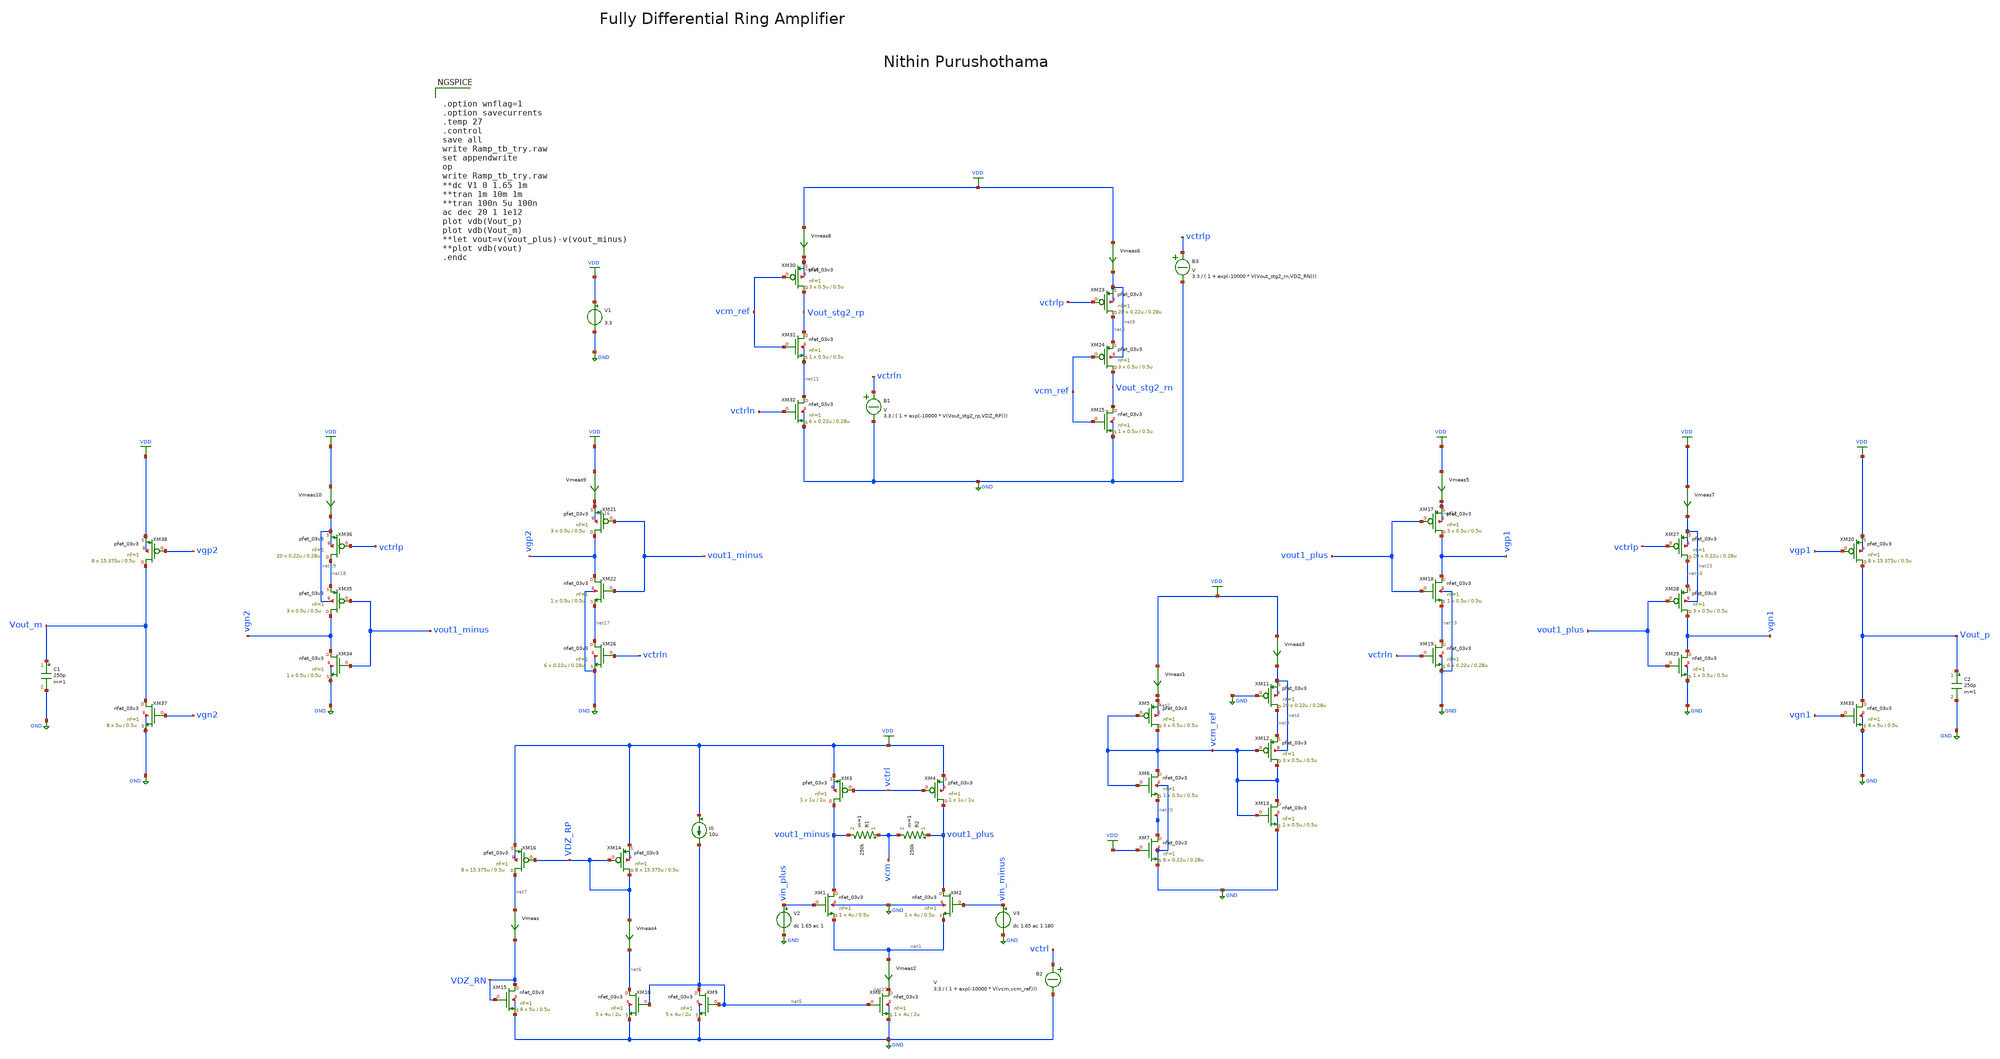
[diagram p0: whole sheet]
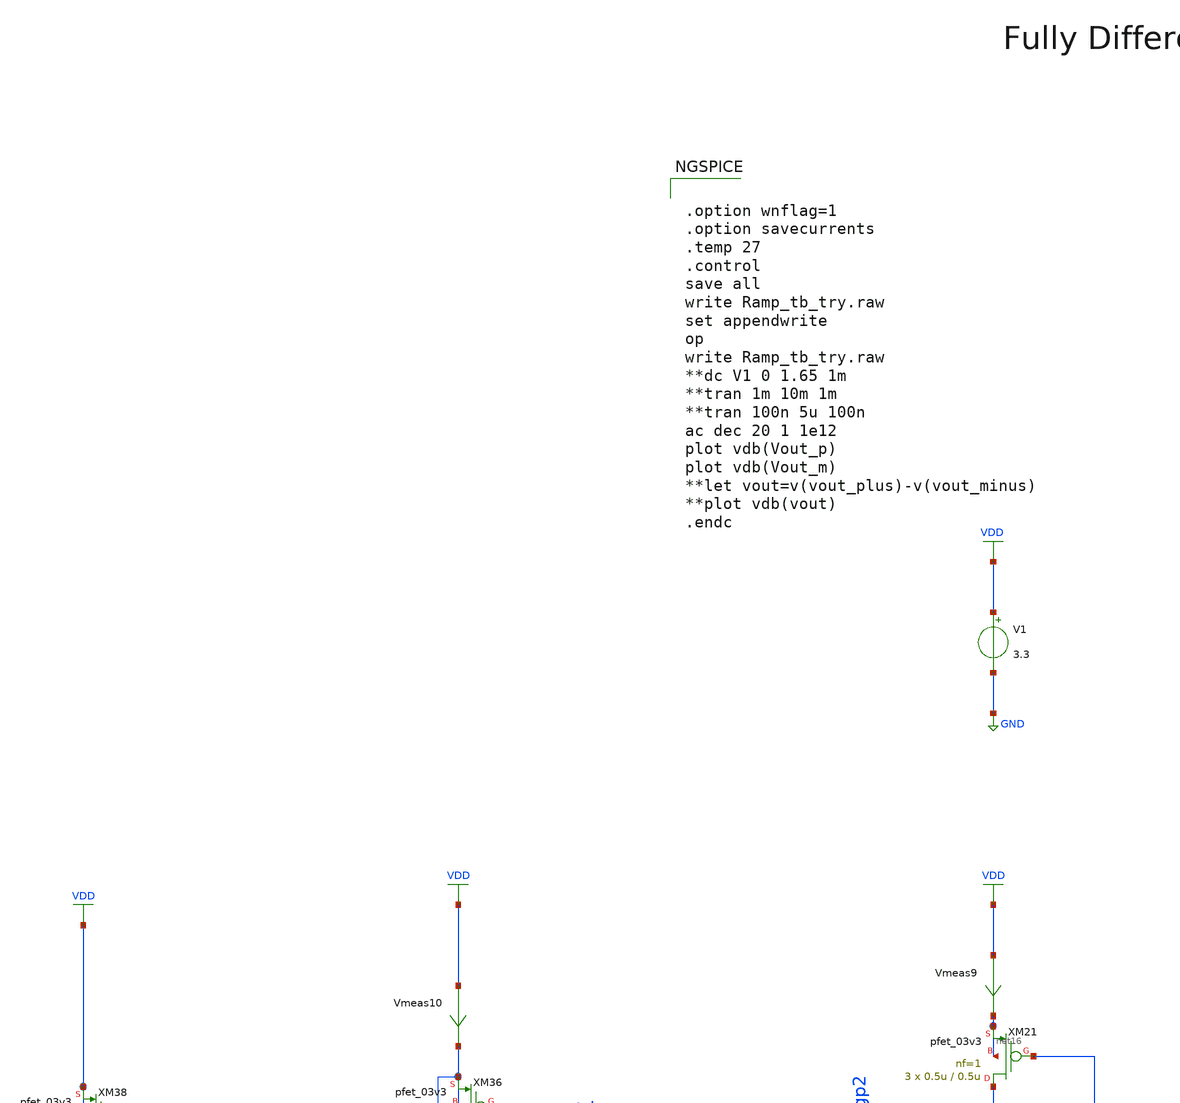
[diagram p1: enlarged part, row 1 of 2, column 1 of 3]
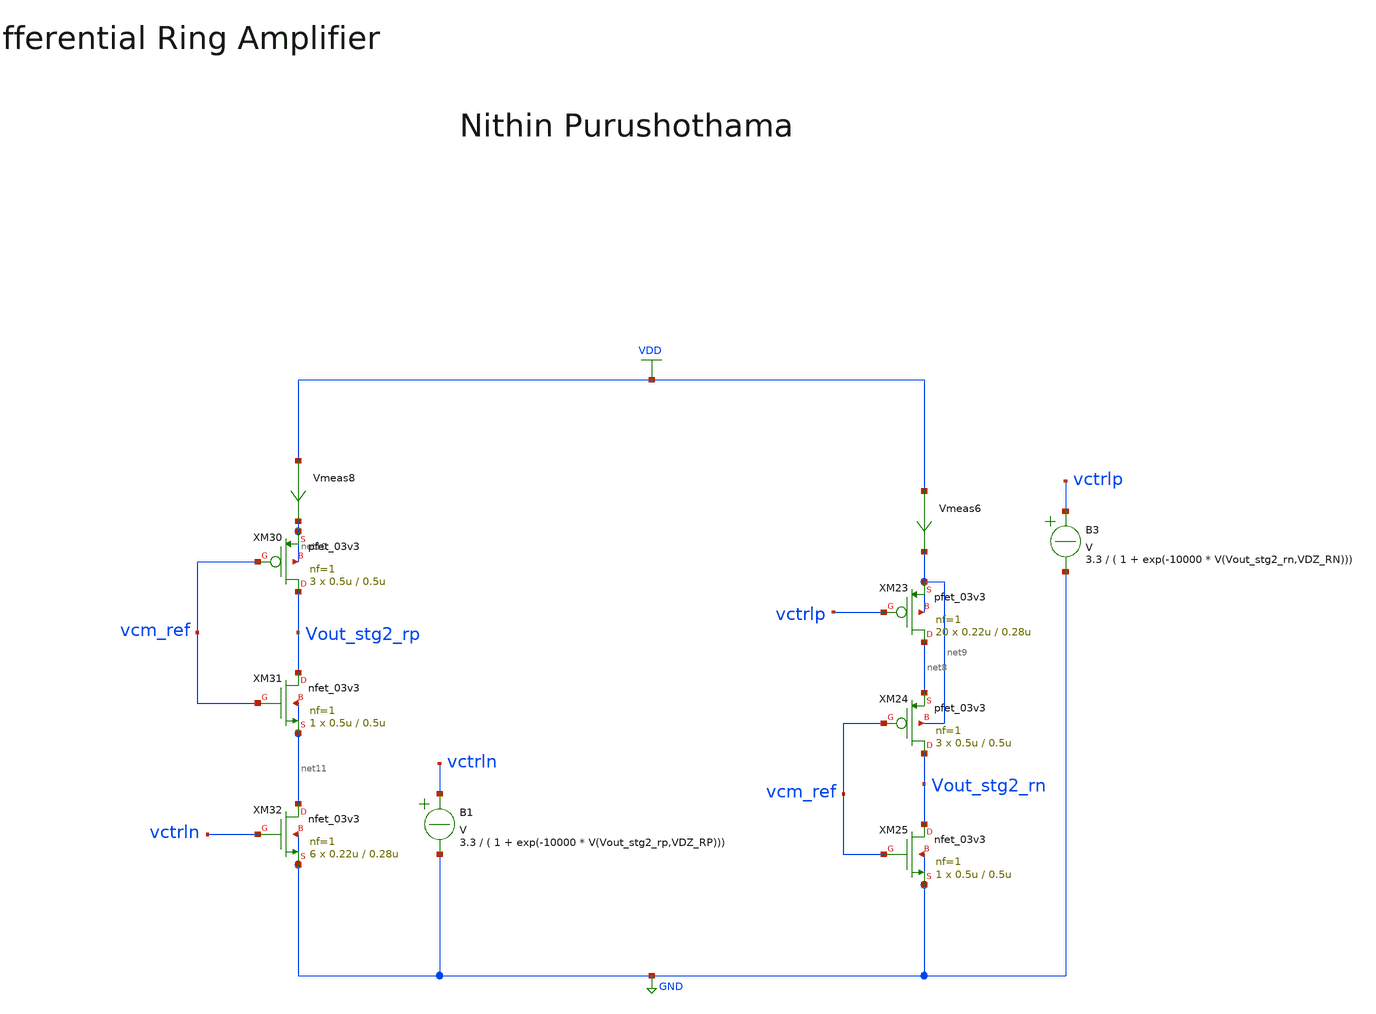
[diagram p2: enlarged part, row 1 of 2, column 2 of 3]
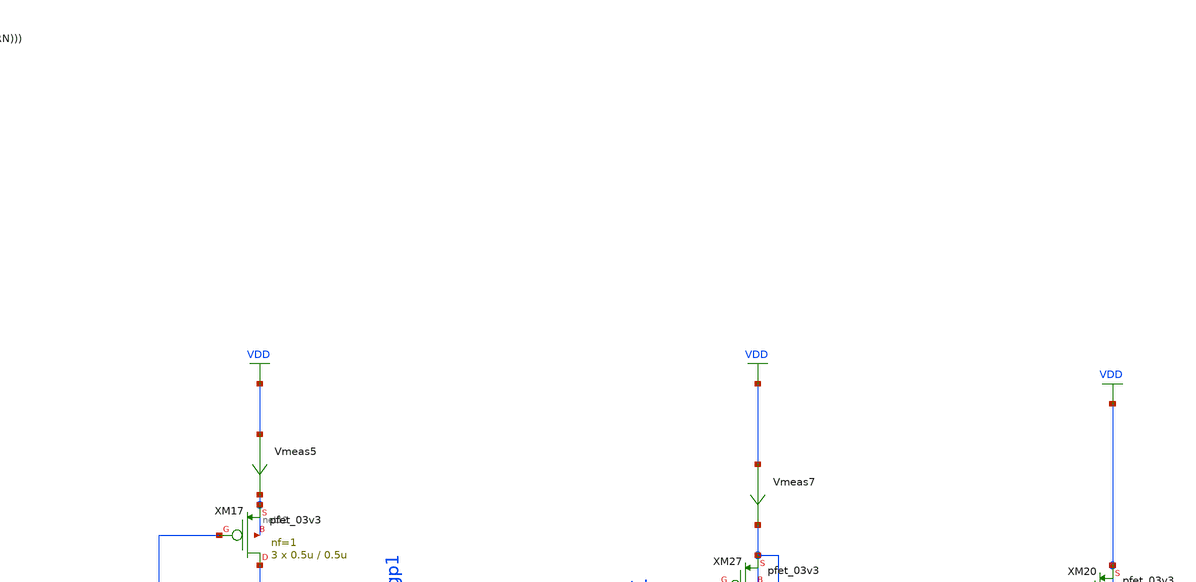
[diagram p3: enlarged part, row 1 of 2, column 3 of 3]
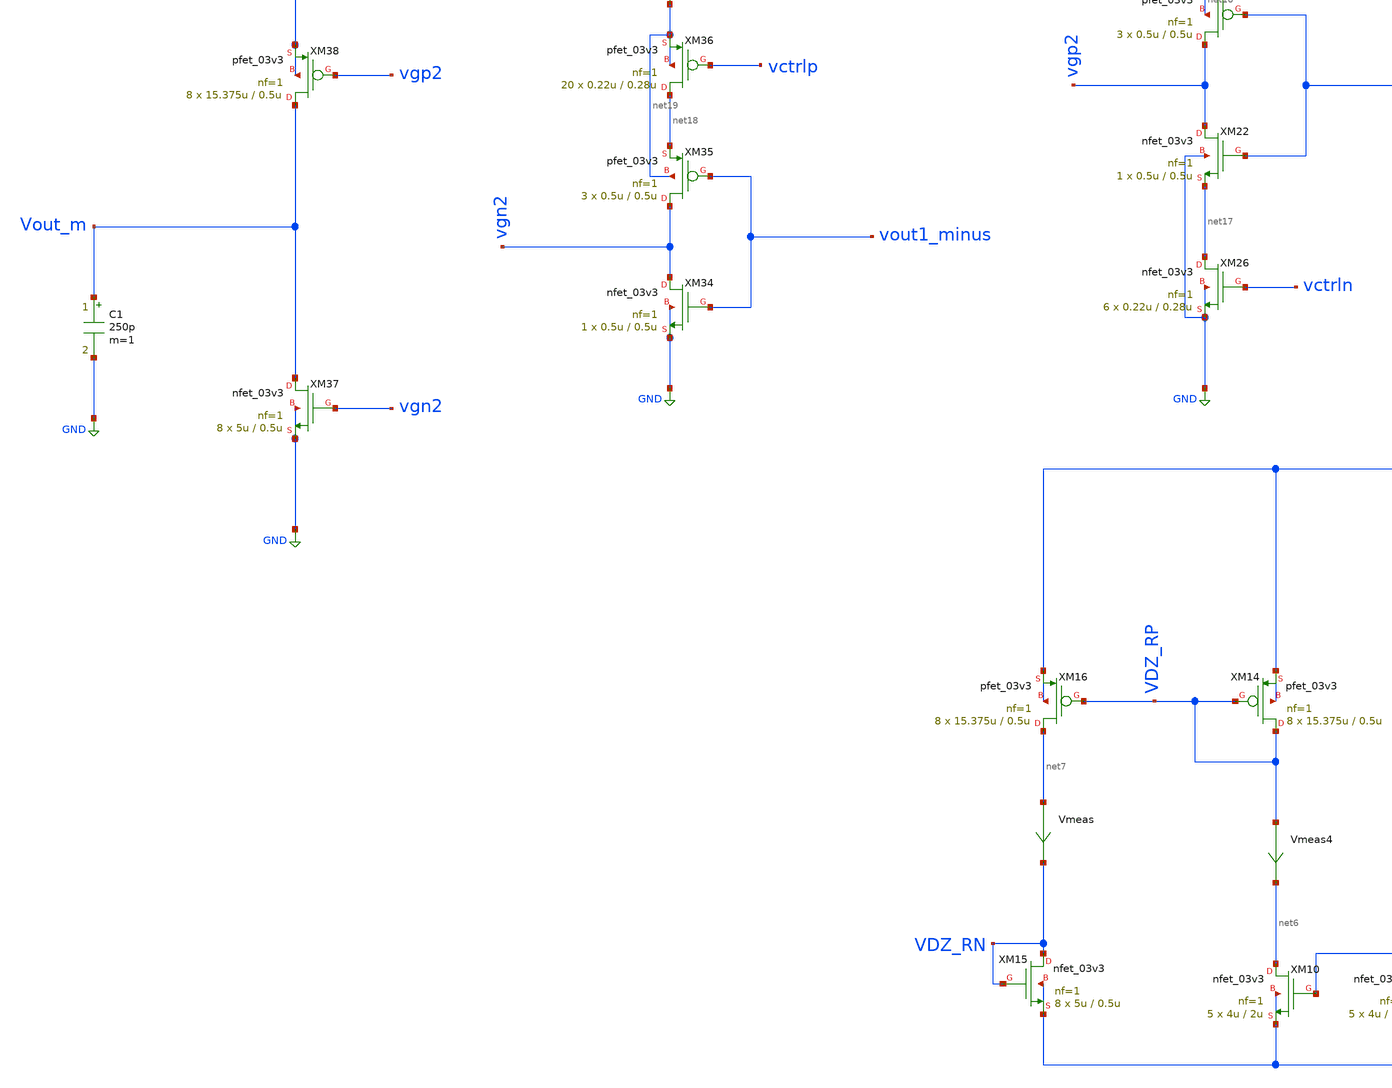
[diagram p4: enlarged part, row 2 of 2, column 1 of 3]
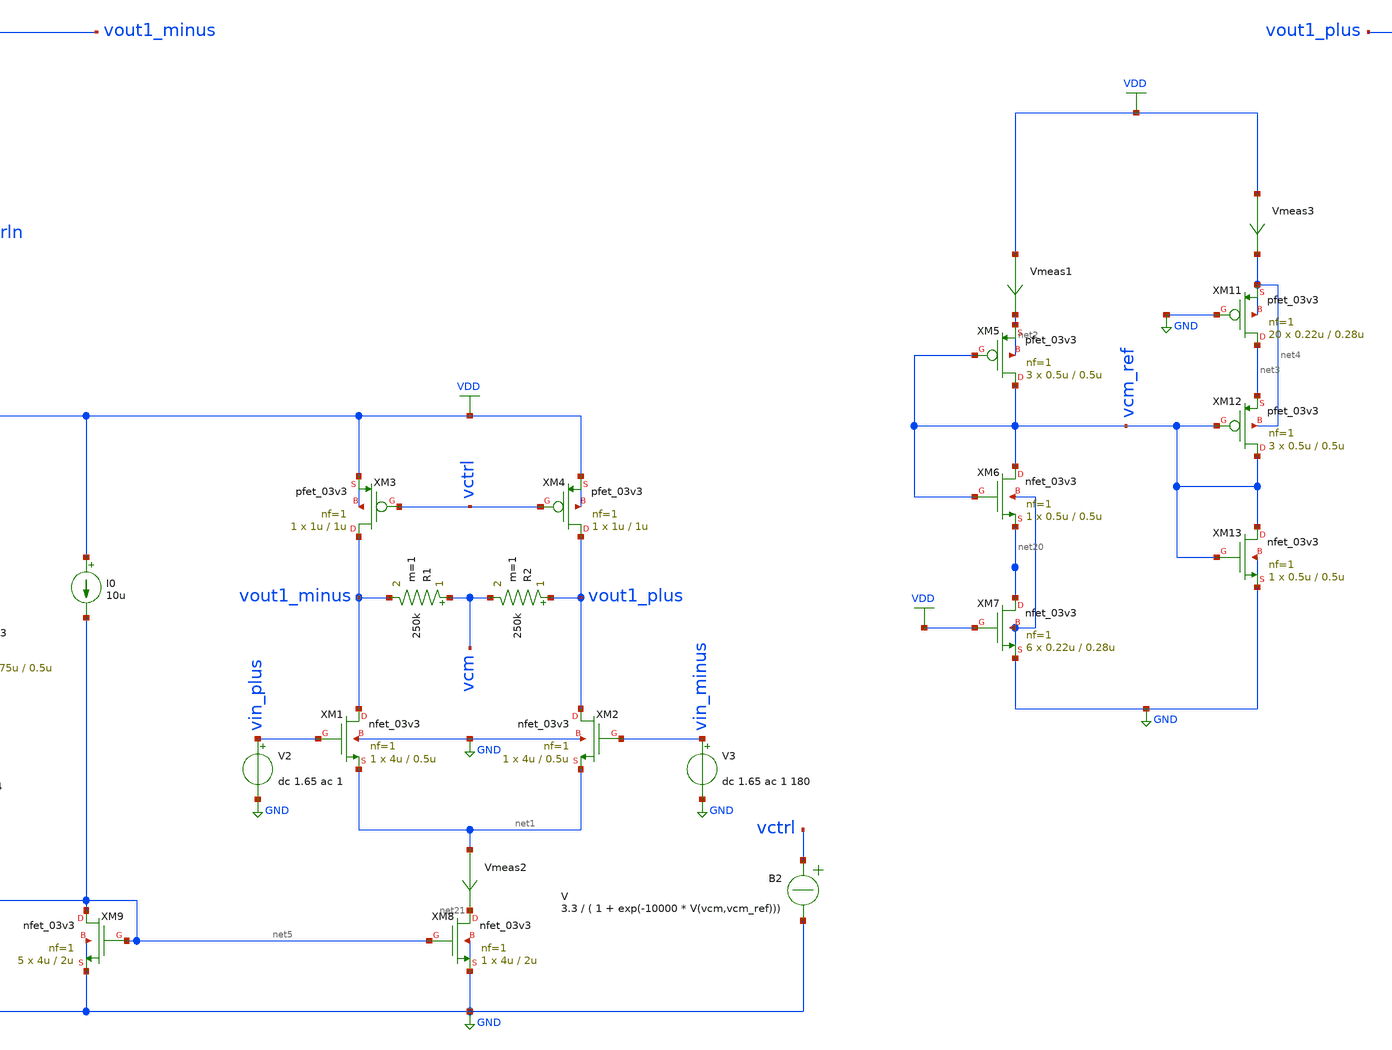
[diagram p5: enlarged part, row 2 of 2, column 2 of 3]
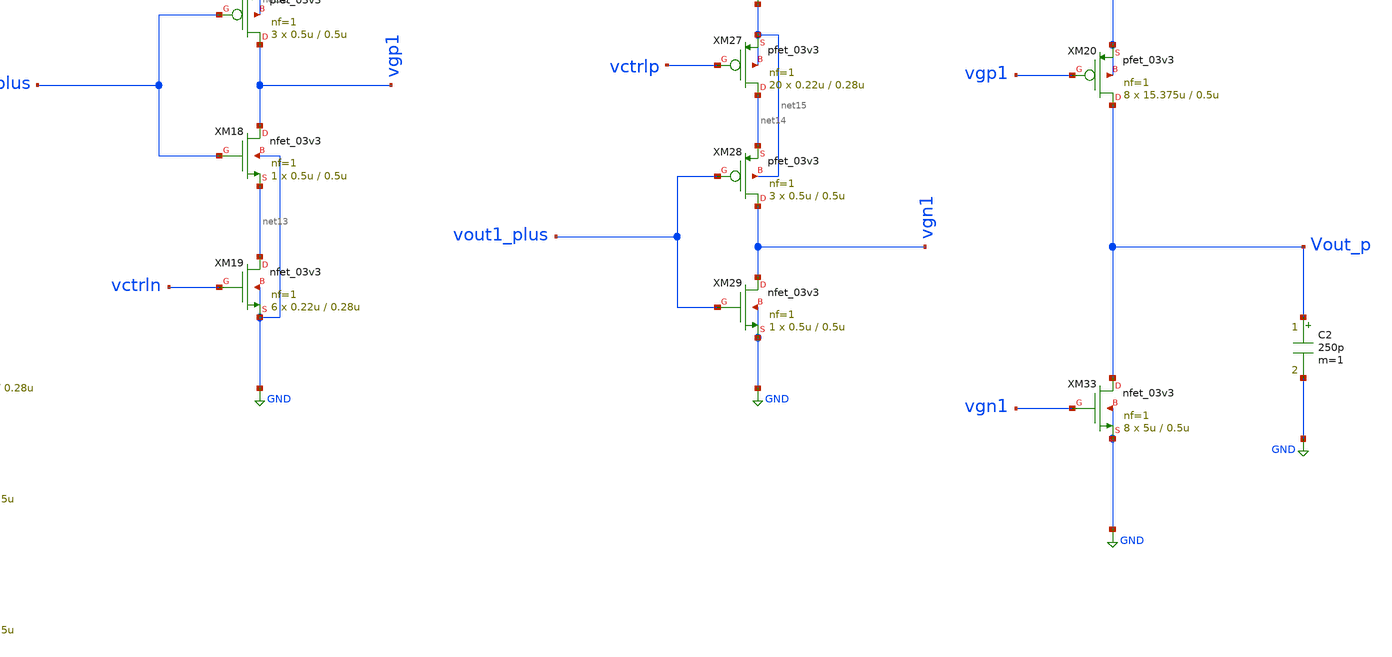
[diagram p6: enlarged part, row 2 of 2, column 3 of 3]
** sch_path: Design_Files/Ring-amp/Ramp_tb_try.sch
**.subckt Ramp_tb_try
XM1 vout1_minus vin_plus net1 GND nfet_03v3 L=0.5u W=4u nf=1 ad='int((nf+1)/2) * W/nf * 0.18u' as='int((nf+2)/2) * W/nf * 0.18u'
+ pd='2*int((nf+1)/2) * (W/nf + 0.18u)' ps='2*int((nf+2)/2) * (W/nf + 0.18u)' nrd='0.18u / W' nrs='0.18u / W'
+ sa=0 sb=0 sd=0 m=1
XM2 vout1_plus vin_minus net1 GND nfet_03v3 L=0.5u W=4u nf=1 ad='int((nf+1)/2) * W/nf * 0.18u' as='int((nf+2)/2) * W/nf * 0.18u'
+ pd='2*int((nf+1)/2) * (W/nf + 0.18u)' ps='2*int((nf+2)/2) * (W/nf + 0.18u)' nrd='0.18u / W' nrs='0.18u / W'
+ sa=0 sb=0 sd=0 m=1
XM3 vout1_minus vctrl VDD VDD pfet_03v3 L=1u W=1u nf=1 ad='int((nf+1)/2) * W/nf * 0.18u' as='int((nf+2)/2) * W/nf * 0.18u'
+ pd='2*int((nf+1)/2) * (W/nf + 0.18u)' ps='2*int((nf+2)/2) * (W/nf + 0.18u)' nrd='0.18u / W' nrs='0.18u / W'
+ sa=0 sb=0 sd=0 m=1
XM4 vout1_plus vctrl VDD VDD pfet_03v3 L=1u W=1u nf=1 ad='int((nf+1)/2) * W/nf * 0.18u' as='int((nf+2)/2) * W/nf * 0.18u'
+ pd='2*int((nf+1)/2) * (W/nf + 0.18u)' ps='2*int((nf+2)/2) * (W/nf + 0.18u)' nrd='0.18u / W' nrs='0.18u / W'
+ sa=0 sb=0 sd=0 m=1
R1 vcm vout1_minus 250k m=1
R2 vout1_plus vcm 250k m=1
Vmeas1 VDD net2 0
.save i(vmeas1)
Vmeas3 VDD net4 0
.save i(vmeas3)
B2 vctrl GND V = 3.3 / ( 1 + exp(-10000 * V(vcm,vcm_ref)))
V2 vin_plus GND dc 1.65 ac 1
XM8 net21 net5 GND GND nfet_03v3 L=2u W=4u nf=1 ad='int((nf+1)/2) * W/nf * 0.18u' as='int((nf+2)/2) * W/nf * 0.18u'
+ pd='2*int((nf+1)/2) * (W/nf + 0.18u)' ps='2*int((nf+2)/2) * (W/nf + 0.18u)' nrd='0.18u / W' nrs='0.18u / W'
+ sa=0 sb=0 sd=0 m=1
XM9 net5 net5 GND GND nfet_03v3 L=2u W=4u nf=1 ad='int((nf+1)/2) * W/nf * 0.18u' as='int((nf+2)/2) * W/nf * 0.18u'
+ pd='2*int((nf+1)/2) * (W/nf + 0.18u)' ps='2*int((nf+2)/2) * (W/nf + 0.18u)' nrd='0.18u / W' nrs='0.18u / W'
+ sa=0 sb=0 sd=0 m=5
I0 VDD net5 10u
Vmeas2 net1 net21 0
.save i(vmeas2)
XM10 net6 net5 GND GND nfet_03v3 L=2u W=4u nf=1 ad='int((nf+1)/2) * W/nf * 0.18u' as='int((nf+2)/2) * W/nf * 0.18u'
+ pd='2*int((nf+1)/2) * (W/nf + 0.18u)' ps='2*int((nf+2)/2) * (W/nf + 0.18u)' nrd='0.18u / W' nrs='0.18u / W'
+ sa=0 sb=0 sd=0 m=5
XM14 VDZ_RP VDZ_RP VDD VDD pfet_03v3 L=0.5u W=15.375u nf=1 ad='int((nf+1)/2) * W/nf * 0.18u' as='int((nf+2)/2) * W/nf * 0.18u'
+ pd='2*int((nf+1)/2) * (W/nf + 0.18u)' ps='2*int((nf+2)/2) * (W/nf + 0.18u)' nrd='0.18u / W' nrs='0.18u / W'
+ sa=0 sb=0 sd=0 m=8
Vmeas4 VDZ_RP net6 0
.save i(vmeas4)
XM15 VDZ_RN VDZ_RN GND GND nfet_03v3 L=0.5u W=5u nf=1 ad='int((nf+1)/2) * W/nf * 0.18u' as='int((nf+2)/2) * W/nf * 0.18u'
+ pd='2*int((nf+1)/2) * (W/nf + 0.18u)' ps='2*int((nf+2)/2) * (W/nf + 0.18u)' nrd='0.18u / W' nrs='0.18u / W'
+ sa=0 sb=0 sd=0 m=8
Vmeas net7 VDZ_RN 0
.save i(vmeas)
XM16 net7 VDZ_RP VDD VDD pfet_03v3 L=0.5u W=15.375u nf=1 ad='int((nf+1)/2) * W/nf * 0.18u' as='int((nf+2)/2) * W/nf * 0.18u'
+ pd='2*int((nf+1)/2) * (W/nf + 0.18u)' ps='2*int((nf+2)/2) * (W/nf + 0.18u)' nrd='0.18u / W' nrs='0.18u / W'
+ sa=0 sb=0 sd=0 m=8
V3 vin_minus GND dc 1.65 ac 1 180
B1 vctrln GND V = 3.3 / ( 1 + exp(-10000 * V(Vout_stg2_rp,VDZ_RP)))
Vmeas6 VDD net9 0
.save i(vmeas6)
B3 vctrlp GND V = 3.3 / ( 1 + exp(-10000 * V(Vout_stg2_rn,VDZ_RN)))
Vmeas8 VDD net10 0
.save i(vmeas8)
Vmeas5 VDD net12 0
.save i(vmeas5)
Vmeas7 VDD net15 0
.save i(vmeas7)
XM33 Vout_p vgn1 GND GND nfet_03v3 L=0.5u W=5u nf=1 ad='int((nf+1)/2) * W/nf * 0.18u' as='int((nf+2)/2) * W/nf * 0.18u'
+ pd='2*int((nf+1)/2) * (W/nf + 0.18u)' ps='2*int((nf+2)/2) * (W/nf + 0.18u)' nrd='0.18u / W' nrs='0.18u / W'
+ sa=0 sb=0 sd=0 m=8
XM20 Vout_p vgp1 VDD VDD pfet_03v3 L=0.5u W=15.375u nf=1 ad='int((nf+1)/2) * W/nf * 0.18u' as='int((nf+2)/2) * W/nf * 0.18u'
+ pd='2*int((nf+1)/2) * (W/nf + 0.18u)' ps='2*int((nf+2)/2) * (W/nf + 0.18u)' nrd='0.18u / W' nrs='0.18u / W'
+ sa=0 sb=0 sd=0 m=8
Vmeas9 VDD net16 0
.save i(vmeas9)
Vmeas10 VDD net19 0
.save i(vmeas10)
XM37 Vout_m vgn2 GND GND nfet_03v3 L=0.5u W=5u nf=1 ad='int((nf+1)/2) * W/nf * 0.18u' as='int((nf+2)/2) * W/nf * 0.18u'
+ pd='2*int((nf+1)/2) * (W/nf + 0.18u)' ps='2*int((nf+2)/2) * (W/nf + 0.18u)' nrd='0.18u / W' nrs='0.18u / W'
+ sa=0 sb=0 sd=0 m=8
XM38 Vout_m vgp2 VDD VDD pfet_03v3 L=0.5u W=15.375u nf=1 ad='int((nf+1)/2) * W/nf * 0.18u' as='int((nf+2)/2) * W/nf * 0.18u'
+ pd='2*int((nf+1)/2) * (W/nf + 0.18u)' ps='2*int((nf+2)/2) * (W/nf + 0.18u)' nrd='0.18u / W' nrs='0.18u / W'
+ sa=0 sb=0 sd=0 m=8
C1 Vout_m GND 250p m=1
C2 Vout_p GND 250p m=1
V1 VDD GND 3.3
XM30 Vout_stg2_rp vcm_ref net10 net10 pfet_03v3 L=0.5u W=0.5u nf=1 ad='int((nf+1)/2) * W/nf * 0.18u'
+ as='int((nf+2)/2) * W/nf * 0.18u' pd='2*int((nf+1)/2) * (W/nf + 0.18u)' ps='2*int((nf+2)/2) * (W/nf + 0.18u)'
+ nrd='0.18u / W' nrs='0.18u / W' sa=0 sb=0 sd=0 m=3
XM31 Vout_stg2_rp vcm_ref net11 net11 nfet_03v3 L=0.5u W=0.5u nf=1 ad='int((nf+1)/2) * W/nf * 0.18u'
+ as='int((nf+2)/2) * W/nf * 0.18u' pd='2*int((nf+1)/2) * (W/nf + 0.18u)' ps='2*int((nf+2)/2) * (W/nf + 0.18u)'
+ nrd='0.18u / W' nrs='0.18u / W' sa=0 sb=0 sd=0 m=1
XM32 net11 vctrln GND GND nfet_03v3 L=0.28u W=0.22u nf=1 ad='int((nf+1)/2) * W/nf * 0.18u' as='int((nf+2)/2) * W/nf * 0.18u'
+ pd='2*int((nf+1)/2) * (W/nf + 0.18u)' ps='2*int((nf+2)/2) * (W/nf + 0.18u)' nrd='0.18u / W' nrs='0.18u / W'
+ sa=0 sb=0 sd=0 m=6
XM23 net8 vctrlp net9 net9 pfet_03v3 L=0.28u W=0.22u nf=1 ad='int((nf+1)/2) * W/nf * 0.18u' as='int((nf+2)/2) * W/nf * 0.18u'
+ pd='2*int((nf+1)/2) * (W/nf + 0.18u)' ps='2*int((nf+2)/2) * (W/nf + 0.18u)' nrd='0.18u / W' nrs='0.18u / W'
+ sa=0 sb=0 sd=0 m=20
XM24 Vout_stg2_rn vcm_ref net8 net9 pfet_03v3 L=0.5u W=0.5u nf=1 ad='int((nf+1)/2) * W/nf * 0.18u' as='int((nf+2)/2) * W/nf * 0.18u'
+ pd='2*int((nf+1)/2) * (W/nf + 0.18u)' ps='2*int((nf+2)/2) * (W/nf + 0.18u)' nrd='0.18u / W' nrs='0.18u / W'
+ sa=0 sb=0 sd=0 m=3
XM25 Vout_stg2_rn vcm_ref GND GND nfet_03v3 L=0.5u W=0.5u nf=1 ad='int((nf+1)/2) * W/nf * 0.18u' as='int((nf+2)/2) * W/nf * 0.18u'
+ pd='2*int((nf+1)/2) * (W/nf + 0.18u)' ps='2*int((nf+2)/2) * (W/nf + 0.18u)' nrd='0.18u / W' nrs='0.18u / W'
+ sa=0 sb=0 sd=0 m=1
XM21 vgp2 vout1_minus net16 net16 pfet_03v3 L=0.5u W=0.5u nf=1 ad='int((nf+1)/2) * W/nf * 0.18u' as='int((nf+2)/2) * W/nf * 0.18u'
+ pd='2*int((nf+1)/2) * (W/nf + 0.18u)' ps='2*int((nf+2)/2) * (W/nf + 0.18u)' nrd='0.18u / W' nrs='0.18u / W'
+ sa=0 sb=0 sd=0 m=3
XM22 vgp2 vout1_minus net17 GND nfet_03v3 L=0.5u W=0.5u nf=1 ad='int((nf+1)/2) * W/nf * 0.18u' as='int((nf+2)/2) * W/nf * 0.18u'
+ pd='2*int((nf+1)/2) * (W/nf + 0.18u)' ps='2*int((nf+2)/2) * (W/nf + 0.18u)' nrd='0.18u / W' nrs='0.18u / W'
+ sa=0 sb=0 sd=0 m=1
XM26 net17 vctrln GND GND nfet_03v3 L=0.28u W=0.22u nf=1 ad='int((nf+1)/2) * W/nf * 0.18u' as='int((nf+2)/2) * W/nf * 0.18u'
+ pd='2*int((nf+1)/2) * (W/nf + 0.18u)' ps='2*int((nf+2)/2) * (W/nf + 0.18u)' nrd='0.18u / W' nrs='0.18u / W'
+ sa=0 sb=0 sd=0 m=6
XM34 vgn2 vout1_minus GND GND nfet_03v3 L=0.5u W=0.5u nf=1 ad='int((nf+1)/2) * W/nf * 0.18u' as='int((nf+2)/2) * W/nf * 0.18u'
+ pd='2*int((nf+1)/2) * (W/nf + 0.18u)' ps='2*int((nf+2)/2) * (W/nf + 0.18u)' nrd='0.18u / W' nrs='0.18u / W'
+ sa=0 sb=0 sd=0 m=1
XM35 vgn2 vout1_minus net18 net19 pfet_03v3 L=0.5u W=0.5u nf=1 ad='int((nf+1)/2) * W/nf * 0.18u' as='int((nf+2)/2) * W/nf * 0.18u'
+ pd='2*int((nf+1)/2) * (W/nf + 0.18u)' ps='2*int((nf+2)/2) * (W/nf + 0.18u)' nrd='0.18u / W' nrs='0.18u / W'
+ sa=0 sb=0 sd=0 m=3
XM36 net18 vctrlp net19 net19 pfet_03v3 L=0.28u W=0.22u nf=1 ad='int((nf+1)/2) * W/nf * 0.18u' as='int((nf+2)/2) * W/nf * 0.18u'
+ pd='2*int((nf+1)/2) * (W/nf + 0.18u)' ps='2*int((nf+2)/2) * (W/nf + 0.18u)' nrd='0.18u / W' nrs='0.18u / W'
+ sa=0 sb=0 sd=0 m=20
XM5 vcm_ref vcm_ref net2 net2 pfet_03v3 L=0.5u W=0.5u nf=1 ad='int((nf+1)/2) * W/nf * 0.18u' as='int((nf+2)/2) * W/nf * 0.18u'
+ pd='2*int((nf+1)/2) * (W/nf + 0.18u)' ps='2*int((nf+2)/2) * (W/nf + 0.18u)' nrd='0.18u / W' nrs='0.18u / W'
+ sa=0 sb=0 sd=0 m=3
XM6 vcm_ref vcm_ref net20 GND nfet_03v3 L=0.5u W=0.5u nf=1 ad='int((nf+1)/2) * W/nf * 0.18u' as='int((nf+2)/2) * W/nf * 0.18u'
+ pd='2*int((nf+1)/2) * (W/nf + 0.18u)' ps='2*int((nf+2)/2) * (W/nf + 0.18u)' nrd='0.18u / W' nrs='0.18u / W'
+ sa=0 sb=0 sd=0 m=1
XM7 net20 VDD GND GND nfet_03v3 L=0.28u W=0.22u nf=1 ad='int((nf+1)/2) * W/nf * 0.18u' as='int((nf+2)/2) * W/nf * 0.18u'
+ pd='2*int((nf+1)/2) * (W/nf + 0.18u)' ps='2*int((nf+2)/2) * (W/nf + 0.18u)' nrd='0.18u / W' nrs='0.18u / W'
+ sa=0 sb=0 sd=0 m=6
XM11 net3 GND net4 net4 pfet_03v3 L=0.28u W=0.22u nf=1 ad='int((nf+1)/2) * W/nf * 0.18u' as='int((nf+2)/2) * W/nf * 0.18u'
+ pd='2*int((nf+1)/2) * (W/nf + 0.18u)' ps='2*int((nf+2)/2) * (W/nf + 0.18u)' nrd='0.18u / W' nrs='0.18u / W'
+ sa=0 sb=0 sd=0 m=20
XM12 vcm_ref vcm_ref net3 net4 pfet_03v3 L=0.5u W=0.5u nf=1 ad='int((nf+1)/2) * W/nf * 0.18u' as='int((nf+2)/2) * W/nf * 0.18u'
+ pd='2*int((nf+1)/2) * (W/nf + 0.18u)' ps='2*int((nf+2)/2) * (W/nf + 0.18u)' nrd='0.18u / W' nrs='0.18u / W'
+ sa=0 sb=0 sd=0 m=3
XM13 vcm_ref vcm_ref GND GND nfet_03v3 L=0.5u W=0.5u nf=1 ad='int((nf+1)/2) * W/nf * 0.18u' as='int((nf+2)/2) * W/nf * 0.18u'
+ pd='2*int((nf+1)/2) * (W/nf + 0.18u)' ps='2*int((nf+2)/2) * (W/nf + 0.18u)' nrd='0.18u / W' nrs='0.18u / W'
+ sa=0 sb=0 sd=0 m=1
XM17 vgp1 vout1_plus net12 net12 pfet_03v3 L=0.5u W=0.5u nf=1 ad='int((nf+1)/2) * W/nf * 0.18u' as='int((nf+2)/2) * W/nf * 0.18u'
+ pd='2*int((nf+1)/2) * (W/nf + 0.18u)' ps='2*int((nf+2)/2) * (W/nf + 0.18u)' nrd='0.18u / W' nrs='0.18u / W'
+ sa=0 sb=0 sd=0 m=3
XM18 vgp1 vout1_plus net13 GND nfet_03v3 L=0.5u W=0.5u nf=1 ad='int((nf+1)/2) * W/nf * 0.18u' as='int((nf+2)/2) * W/nf * 0.18u'
+ pd='2*int((nf+1)/2) * (W/nf + 0.18u)' ps='2*int((nf+2)/2) * (W/nf + 0.18u)' nrd='0.18u / W' nrs='0.18u / W'
+ sa=0 sb=0 sd=0 m=1
XM19 net13 vctrln GND GND nfet_03v3 L=0.28u W=0.22u nf=1 ad='int((nf+1)/2) * W/nf * 0.18u' as='int((nf+2)/2) * W/nf * 0.18u'
+ pd='2*int((nf+1)/2) * (W/nf + 0.18u)' ps='2*int((nf+2)/2) * (W/nf + 0.18u)' nrd='0.18u / W' nrs='0.18u / W'
+ sa=0 sb=0 sd=0 m=6
XM27 net14 vctrlp net15 net15 pfet_03v3 L=0.28u W=0.22u nf=1 ad='int((nf+1)/2) * W/nf * 0.18u' as='int((nf+2)/2) * W/nf * 0.18u'
+ pd='2*int((nf+1)/2) * (W/nf + 0.18u)' ps='2*int((nf+2)/2) * (W/nf + 0.18u)' nrd='0.18u / W' nrs='0.18u / W'
+ sa=0 sb=0 sd=0 m=20
XM28 vgn1 vout1_plus net14 net15 pfet_03v3 L=0.5u W=0.5u nf=1 ad='int((nf+1)/2) * W/nf * 0.18u' as='int((nf+2)/2) * W/nf * 0.18u'
+ pd='2*int((nf+1)/2) * (W/nf + 0.18u)' ps='2*int((nf+2)/2) * (W/nf + 0.18u)' nrd='0.18u / W' nrs='0.18u / W'
+ sa=0 sb=0 sd=0 m=3
XM29 vgn1 vout1_plus GND GND nfet_03v3 L=0.5u W=0.5u nf=1 ad='int((nf+1)/2) * W/nf * 0.18u' as='int((nf+2)/2) * W/nf * 0.18u'
+ pd='2*int((nf+1)/2) * (W/nf + 0.18u)' ps='2*int((nf+2)/2) * (W/nf + 0.18u)' nrd='0.18u / W' nrs='0.18u / W'
+ sa=0 sb=0 sd=0 m=1
**** begin user architecture code


.option wnflag=1
.option savecurrents
.temp 27
.control
save all
write Ramp_tb_try.raw
set appendwrite
op
write Ramp_tb_try.raw
**dc V1 0 1.65 1m
**tran 1m 10m 1m
**tran 100n 5u 100n
ac dec 20 1 1e12
plot vdb(Vout_p)
plot vdb(Vout_m)
**let vout=v(vout_plus)-v(vout_minus)
**plot vdb(vout)
.endc




.save @m.xm1.m0[gm]
.save @m.xm1.m0[id]
.save @m.xm1.m0[vth]
.save @m.xm1.m0[vds]
.save @m.xm1.m0[gds]
.save @m.xm1.m0[cgg]
.save @m.xm1.m0[cgs]
.save @m.xm1.m0[cgd]
.save @m.xm2.m0[gm]
.save @m.xm2.m0[id]
.save @m.xm2.m0[vth]
.save @m.xm2.m0[vds]
.save @m.xm2.m0[gds]
.save @m.xm2.m0[cgg]
.save @m.xm2.m0[cgs]
.save @m.xm2.m0[cgd]
.save @m.xm3.m0[gm]
.save @m.xm3.m0[id]
.save @m.xm3.m0[vth]
.save @m.xm3.m0[vds]
.save @m.xm3.m0[gds]
.save @m.xm3.m0[cgg]
.save @m.xm3.m0[cgs]
.save @m.xm3.m0[cgd]
.save @m.xm4.m0[gm]
.save @m.xm4.m0[id]
.save @m.xm4.m0[vth]
.save @m.xm4.m0[vds]
.save @m.xm4.m0[gds]
.save @m.xm4.m0[cgg]
.save @m.xm4.m0[cgs]
.save @m.xm4.m0[cgd]
.save @m.xm5.m0[gm]
.save @m.xm5.m0[id]
.save @m.xm5.m0[vth]
.save @m.xm5.m0[vds]
.save @m.xm5.m0[gds]
.save @m.xm5.m0[cgg]
.save @m.xm5.m0[cgs]
.save @m.xm5.m0[cgd]
.save @m.xm6.m0[gm]
.save @m.xm6.m0[id]
.save @m.xm6.m0[vth]
.save @m.xm6.m0[vds]
.save @m.xm6.m0[gds]
.save @m.xm6.m0[cgg]
.save @m.xm6.m0[cgs]
.save @m.xm6.m0[cgd]
.save @m.xm7.m0[gm]
.save @m.xm7.m0[id]
.save @m.xm7.m0[vth]
.save @m.xm7.m0[vds]
.save @m.xm7.m0[gds]
.save @m.xm7.m0[cgg]
.save @m.xm7.m0[cgs]
.save @m.xm7.m0[cgd]
.save @m.xm8.m0[gm]
.save @m.xm8.m0[id]
.save @m.xm8.m0[vth]
.save @m.xm8.m0[vds]
.save @m.xm8.m0[gds]
.save @m.xm8.m0[cgg]
.save @m.xm8.m0[cgs]
.save @m.xm8.m0[cgd]
.save @m.xm9.m0[gm]
.save @m.xm9.m0[id]
.save @m.xm9.m0[vth]
.save @m.xm9.m0[vds]
.save @m.xm9.m0[gds]
.save @m.xm9.m0[cgg]
.save @m.xm9.m0[cgs]
.save @m.xm9.m0[cgd]
.save @m.xm10.m0[gm]
.save @m.xm10.m0[id]
.save @m.xm10.m0[vth]
.save @m.xm10.m0[vds]
.save @m.xm10.m0[gds]
.save @m.xm10.m0[cgg]
.save @m.xm10.m0[cgs]
.save @m.xm10.m0[cgd]
.save @m.xm11.m0[gm]
.save @m.xm11.m0[id]
.save @m.xm11.m0[vth]
.save @m.xm11.m0[vds]
.save @m.xm11.m0[gds]
.save @m.xm11.m0[cgg]
.save @m.xm11.m0[cgs]
.save @m.xm11.m0[cgd]
.save @m.xm12.m0[gm]
.save @m.xm12.m0[id]
.save @m.xm12.m0[vth]
.save @m.xm12.m0[vds]
.save @m.xm12.m0[gds]
.save @m.xm12.m0[cgg]
.save @m.xm12.m0[cgs]
.save @m.xm12.m0[cgd]
.save @m.xm13.m0[gm]
.save @m.xm13.m0[id]
.save @m.xm13.m0[vth]
.save @m.xm13.m0[vds]
.save @m.xm13.m0[gds]
.save @m.xm13.m0[cgg]
.save @m.xm13.m0[cgs]
.save @m.xm13.m0[cgd]
.save @m.xm14.m0[gm]
.save @m.xm14.m0[id]
.save @m.xm14.m0[vth]
.save @m.xm14.m0[vds]
.save @m.xm14.m0[gds]
.save @m.xm14.m0[cgg]
.save @m.xm14.m0[cgs]
.save @m.xm14.m0[cgd]
.save @m.xm15.m0[gm]
.save @m.xm15.m0[id]
.save @m.xm15.m0[vth]
.save @m.xm15.m0[vds]
.save @m.xm15.m0[gds]
.save @m.xm15.m0[cgg]
.save @m.xm15.m0[cgs]
.save @m.xm15.m0[cgd]
.save @m.xm16.m0[gm]
.save @m.xm16.m0[id]
.save @m.xm16.m0[vth]
.save @m.xm16.m0[vds]
.save @m.xm16.m0[gds]
.save @m.xm16.m0[cgg]
.save @m.xm16.m0[cgs]
.save @m.xm16.m0[cgd]
.save @m.xm17.m0[gm]
.save @m.xm17.m0[id]
.save @m.xm17.m0[vth]
.save @m.xm17.m0[vds]
.save @m.xm17.m0[gds]
.save @m.xm17.m0[cgg]
.save @m.xm17.m0[cgs]
.save @m.xm17.m0[cgd]
.save @m.xm18.m0[gm]
.save @m.xm18.m0[id]
.save @m.xm18.m0[vth]
.save @m.xm18.m0[vds]
.save @m.xm18.m0[gds]
.save @m.xm18.m0[cgg]
.save @m.xm18.m0[cgs]
.save @m.xm18.m0[cgd]
.save @m.xm19.m0[gm]
.save @m.xm19.m0[id]
.save @m.xm19.m0[vth]
.save @m.xm19.m0[vds]
.save @m.xm19.m0[gds]
.save @m.xm19.m0[cgg]
.save @m.xm19.m0[cgs]
.save @m.xm19.m0[cgd]
.save @m.xm20.m0[gm]
.save @m.xm20.m0[id]
.save @m.xm20.m0[vth]
.save @m.xm20.m0[vds]
.save @m.xm20.m0[gds]
.save @m.xm20.m0[cgg]
.save @m.xm20.m0[cgs]
.save @m.xm20.m0[cgd]
.save @m.xm21.m0[gm]
.save @m.xm21.m0[id]
.save @m.xm21.m0[vth]
.save @m.xm21.m0[vds]
.save @m.xm21.m0[gds]
.save @m.xm21.m0[cgg]
.save @m.xm21.m0[cgs]
.save @m.xm21.m0[cgd]
.save @m.xm22.m0[gm]
.save @m.xm22.m0[id]
.save @m.xm22.m0[vth]
.save @m.xm22.m0[vds]
.save @m.xm22.m0[gds]
.save @m.xm22.m0[cgg]
.save @m.xm22.m0[cgs]
.save @m.xm22.m0[cgd]
.save @m.xm23.m0[gm]
.save @m.xm23.m0[id]
.save @m.xm23.m0[vth]
.save @m.xm23.m0[vds]
.save @m.xm23.m0[gds]
.save @m.xm23.m0[cgg]
.save @m.xm23.m0[cgs]
.save @m.xm23.m0[cgd]
.save @m.xm24.m0[gm]
.save @m.xm24.m0[id]
.save @m.xm24.m0[vth]
.save @m.xm24.m0[vds]
.save @m.xm24.m0[gds]
.save @m.xm24.m0[cgg]
.save @m.xm24.m0[cgs]
.save @m.xm24.m0[cgd]
.save @m.xm25.m0[gm]
.save @m.xm25.m0[id]
.save @m.xm25.m0[vth]
.save @m.xm25.m0[vds]
.save @m.xm25.m0[gds]
.save @m.xm25.m0[cgg]
.save @m.xm25.m0[cgs]
.save @m.xm25.m0[cgd]
.save @m.xm26.m0[gm]
.save @m.xm26.m0[id]
.save @m.xm26.m0[vth]
.save @m.xm26.m0[vds]
.save @m.xm26.m0[gds]
.save @m.xm26.m0[cgg]
.save @m.xm26.m0[cgs]
.save @m.xm26.m0[cgd]
.save @m.xm27.m0[gm]
.save @m.xm27.m0[id]
.save @m.xm27.m0[vth]
.save @m.xm27.m0[vds]
.save @m.xm27.m0[gds]
.save @m.xm27.m0[cgg]
.save @m.xm27.m0[cgs]
.save @m.xm27.m0[cgd]
.save @m.xm28.m0[gm]
.save @m.xm28.m0[id]
.save @m.xm28.m0[vth]
.save @m.xm28.m0[vds]
.save @m.xm28.m0[gds]
.save @m.xm28.m0[cgg]
.save @m.xm28.m0[cgs]
.save @m.xm28.m0[cgd]
.save @m.xm29.m0[gm]
.save @m.xm29.m0[id]
.save @m.xm29.m0[vth]
.save @m.xm29.m0[vds]
.save @m.xm29.m0[gds]
.save @m.xm29.m0[cgg]
.save @m.xm29.m0[cgs]
.save @m.xm29.m0[cgd]
.save @m.xm30.m0[gm]
.save @m.xm30.m0[id]
.save @m.xm30.m0[vth]
.save @m.xm30.m0[vds]
.save @m.xm30.m0[gds]
.save @m.xm30.m0[cgg]
.save @m.xm30.m0[cgs]
.save @m.xm30.m0[cgd]
.save @m.xm31.m0[gm]
.save @m.xm31.m0[id]
.save @m.xm31.m0[vth]
.save @m.xm31.m0[vds]
.save @m.xm31.m0[gds]
.save @m.xm31.m0[cgg]
.save @m.xm31.m0[cgs]
.save @m.xm31.m0[cgd]
.save @m.xm32.m0[gm]
.save @m.xm32.m0[id]
.save @m.xm32.m0[vth]
.save @m.xm32.m0[vds]
.save @m.xm32.m0[gds]
.save @m.xm32.m0[cgg]
.save @m.xm32.m0[cgs]
.save @m.xm32.m0[cgd]
.save @m.xm33.m0[gm]
.save @m.xm33.m0[id]
.save @m.xm33.m0[vth]
.save @m.xm33.m0[vds]
.save @m.xm33.m0[gds]
.save @m.xm33.m0[cgg]
.save @m.xm33.m0[cgs]
.save @m.xm33.m0[cgd]
.save @m.xm34.m0[gm]
.save @m.xm34.m0[id]
.save @m.xm34.m0[vth]
.save @m.xm34.m0[vds]
.save @m.xm34.m0[gds]
.save @m.xm34.m0[cgg]
.save @m.xm34.m0[cgs]
.save @m.xm34.m0[cgd]
.save @m.xm35.m0[gm]
.save @m.xm35.m0[id]
.save @m.xm35.m0[vth]
.save @m.xm35.m0[vds]
.save @m.xm35.m0[gds]
.save @m.xm35.m0[cgg]
.save @m.xm35.m0[cgs]
.save @m.xm35.m0[cgd]
.save @m.xm36.m0[gm]
.save @m.xm36.m0[id]
.save @m.xm36.m0[vth]
.save @m.xm36.m0[vds]
.save @m.xm36.m0[gds]
.save @m.xm36.m0[cgg]
.save @m.xm36.m0[cgs]
.save @m.xm36.m0[cgd]
.save @m.xm37.m0[gm]
.save @m.xm37.m0[id]
.save @m.xm37.m0[vth]
.save @m.xm37.m0[vds]
.save @m.xm37.m0[gds]
.save @m.xm37.m0[cgg]
.save @m.xm37.m0[cgs]
.save @m.xm37.m0[cgd]
.save @m.xm38.m0[gm]
.save @m.xm38.m0[id]
.save @m.xm38.m0[vth]
.save @m.xm38.m0[vds]
.save @m.xm38.m0[gds]
.save @m.xm38.m0[cgg]
.save @m.xm38.m0[cgs]
.save @m.xm38.m0[cgd]



.lib /foss/pdks/volare/gf180mcu/versions/0fe599b2afb6708d281543108caf8310912f54af/gf180mcuD/libs.tech/ngspice/sm141064.ngspice typical
.include /foss/pdks/volare/gf180mcu/versions/0fe599b2afb6708d281543108caf8310912f54af/gf180mcuD/libs.tech/ngspice/design.ngspice
.lib /foss/pdks/volare/gf180mcu/versions/0fe599b2afb6708d281543108caf8310912f54af/gf180mcuD/libs.tech/ngspice/sm141064.ngspice res_statistical

**.include $::180MCU_MODELS/design.ngspice
**.lib $::180MCU_MODELS/sm141064.ngspice typical
**.lib $::180MCU_MODELS/sm141064.ngspice res_typical
* .lib $::180MCU_MODELS/sm141064.ngspice res_statistical
*.include $::180MCU_MODELS/design.ngspice
*.lib $::180MCU_MODELS/sm141064.ngspice typical


**** end user architecture code
**.ends
.GLOBAL VDD
.GLOBAL GND
.end
